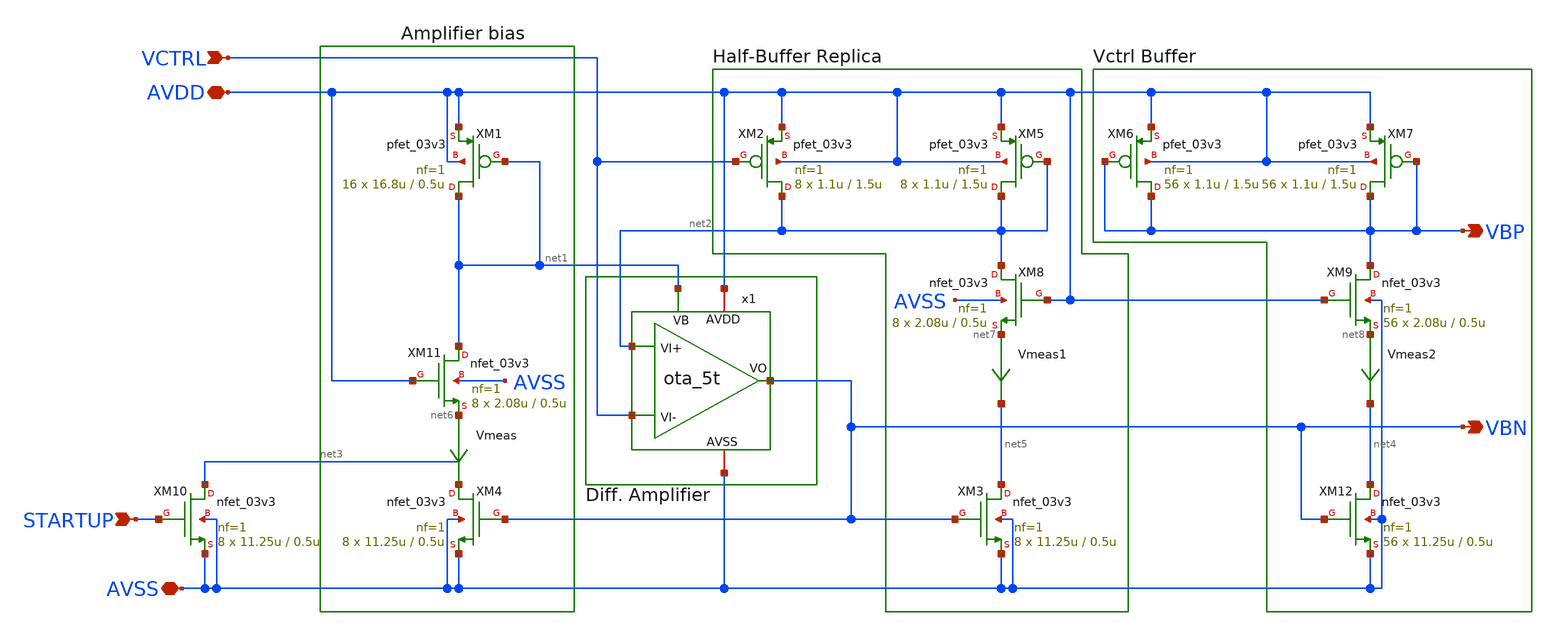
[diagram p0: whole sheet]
** sch_path: designs/libs/core_analog/bias_generator/bias_generator.sch
**.subckt bias_generator VCTRL STARTUP AVDD AVSS VBP VBN
*.ipin VCTRL
*.ipin STARTUP
*.iopin AVDD
*.iopin AVSS
*.opin VBP
*.opin VBN
x1 VBN AVDD net2 VCTRL AVSS net1 ota_5t
Vmeas net6 net3 0
.save i(vmeas)
Vmeas1 net7 net5 0
.save i(vmeas1)
Vmeas2 net8 net4 0
.save i(vmeas2)
XM1 net1 net1 AVDD AVDD pfet_03v3 L=0.5u W=16.8u nf=1 ad='int((nf+1)/2) * W/nf * 0.18u' as='int((nf+2)/2) * W/nf * 0.18u'
+ pd='2*int((nf+1)/2) * (W/nf + 0.18u)' ps='2*int((nf+2)/2) * (W/nf + 0.18u)' nrd='0.18u / W' nrs='0.18u / W'
+ sa=0 sb=0 sd=0 m=16
XM8 net2 AVDD net7 AVSS nfet_03v3 L=0.5u W=2.08u nf=1 ad='int((nf+1)/2) * W/nf * 0.18u' as='int((nf+2)/2) * W/nf * 0.18u'
+ pd='2*int((nf+1)/2) * (W/nf + 0.18u)' ps='2*int((nf+2)/2) * (W/nf + 0.18u)' nrd='0.18u / W' nrs='0.18u / W'
+ sa=0 sb=0 sd=0 m=8
XM9 VBP AVDD net8 AVSS nfet_03v3 L=0.5u W=2.08u nf=1 ad='int((nf+1)/2) * W/nf * 0.18u' as='int((nf+2)/2) * W/nf * 0.18u'
+ pd='2*int((nf+1)/2) * (W/nf + 0.18u)' ps='2*int((nf+2)/2) * (W/nf + 0.18u)' nrd='0.18u / W' nrs='0.18u / W'
+ sa=0 sb=0 sd=0 m=56
XM11 net1 AVDD net6 AVSS nfet_03v3 L=0.5u W=2.08u nf=1 ad='int((nf+1)/2) * W/nf * 0.18u' as='int((nf+2)/2) * W/nf * 0.18u'
+ pd='2*int((nf+1)/2) * (W/nf + 0.18u)' ps='2*int((nf+2)/2) * (W/nf + 0.18u)' nrd='0.18u / W' nrs='0.18u / W'
+ sa=0 sb=0 sd=0 m=8
XM12 net4 VBN AVSS AVSS nfet_03v3 L=0.5u W=11.25u nf=1 ad='int((nf+1)/2) * W/nf * 0.18u' as='int((nf+2)/2) * W/nf * 0.18u'
+ pd='2*int((nf+1)/2) * (W/nf + 0.18u)' ps='2*int((nf+2)/2) * (W/nf + 0.18u)' nrd='0.18u / W' nrs='0.18u / W'
+ sa=0 sb=0 sd=0 m=56
XM3 net5 VBN AVSS AVSS nfet_03v3 L=0.5u W=11.25u nf=1 ad='int((nf+1)/2) * W/nf * 0.18u' as='int((nf+2)/2) * W/nf * 0.18u'
+ pd='2*int((nf+1)/2) * (W/nf + 0.18u)' ps='2*int((nf+2)/2) * (W/nf + 0.18u)' nrd='0.18u / W' nrs='0.18u / W'
+ sa=0 sb=0 sd=0 m=8
XM4 net3 VBN AVSS AVSS nfet_03v3 L=0.5u W=11.25u nf=1 ad='int((nf+1)/2) * W/nf * 0.18u' as='int((nf+2)/2) * W/nf * 0.18u'
+ pd='2*int((nf+1)/2) * (W/nf + 0.18u)' ps='2*int((nf+2)/2) * (W/nf + 0.18u)' nrd='0.18u / W' nrs='0.18u / W'
+ sa=0 sb=0 sd=0 m=8
XM10 net3 STARTUP AVSS AVSS nfet_03v3 L=0.5u W=11.25u nf=1 ad='int((nf+1)/2) * W/nf * 0.18u' as='int((nf+2)/2) * W/nf * 0.18u'
+ pd='2*int((nf+1)/2) * (W/nf + 0.18u)' ps='2*int((nf+2)/2) * (W/nf + 0.18u)' nrd='0.18u / W' nrs='0.18u / W'
+ sa=0 sb=0 sd=0 m=8
XM2 net2 VCTRL AVDD AVDD pfet_03v3 L=1.5u W=1.1u nf=1 ad='int((nf+1)/2) * W/nf * 0.18u' as='int((nf+2)/2) * W/nf * 0.18u'
+ pd='2*int((nf+1)/2) * (W/nf + 0.18u)' ps='2*int((nf+2)/2) * (W/nf + 0.18u)' nrd='0.18u / W' nrs='0.18u / W'
+ sa=0 sb=0 sd=0 m=8
XM5 net2 net2 AVDD AVDD pfet_03v3 L=1.5u W=1.1u nf=1 ad='int((nf+1)/2) * W/nf * 0.18u' as='int((nf+2)/2) * W/nf * 0.18u'
+ pd='2*int((nf+1)/2) * (W/nf + 0.18u)' ps='2*int((nf+2)/2) * (W/nf + 0.18u)' nrd='0.18u / W' nrs='0.18u / W'
+ sa=0 sb=0 sd=0 m=8
XM6 VBP VBP AVDD AVDD pfet_03v3 L=1.5u W=1.1u nf=1 ad='int((nf+1)/2) * W/nf * 0.18u' as='int((nf+2)/2) * W/nf * 0.18u'
+ pd='2*int((nf+1)/2) * (W/nf + 0.18u)' ps='2*int((nf+2)/2) * (W/nf + 0.18u)' nrd='0.18u / W' nrs='0.18u / W'
+ sa=0 sb=0 sd=0 m=56
XM7 VBP VBP AVDD AVDD pfet_03v3 L=1.5u W=1.1u nf=1 ad='int((nf+1)/2) * W/nf * 0.18u' as='int((nf+2)/2) * W/nf * 0.18u'
+ pd='2*int((nf+1)/2) * (W/nf + 0.18u)' ps='2*int((nf+2)/2) * (W/nf + 0.18u)' nrd='0.18u / W' nrs='0.18u / W'
+ sa=0 sb=0 sd=0 m=56
**.ends

* expanding   symbol:  libs/core_analog/ota_5t/ota_5t.sym # of pins=6
** sym_path: designs/libs/core_analog/ota_5t/ota_5t.sym
** sch_path: designs/libs/core_analog/ota_5t/ota_5t.sch
.subckt ota_5t VO AVDD VI+ VI- AVSS VB
*.ipin VI+
*.ipin VI-
*.ipin VB
*.iopin AVDD
*.iopin AVSS
*.opin VO
XM1 VO VI- net2 AVDD pfet_03v3 L=0.5u W=6.55u nf=1 ad='int((nf+1)/2) * W/nf * 0.18u' as='int((nf+2)/2) * W/nf * 0.18u'
+ pd='2*int((nf+1)/2) * (W/nf + 0.18u)' ps='2*int((nf+2)/2) * (W/nf + 0.18u)' nrd='0.18u / W' nrs='0.18u / W'
+ sa=0 sb=0 sd=0 m=8
XM4 VO net1 AVSS AVSS nfet_03v3 L=0.5u W=4.8u nf=1 ad='int((nf+1)/2) * W/nf * 0.18u' as='int((nf+2)/2) * W/nf * 0.18u'
+ pd='2*int((nf+1)/2) * (W/nf + 0.18u)' ps='2*int((nf+2)/2) * (W/nf + 0.18u)' nrd='0.18u / W' nrs='0.18u / W'
+ sa=0 sb=0 sd=0 m=4
XM3 net2 VB net3 AVDD pfet_03v3 L=0.5u W=16.8u nf=1 ad='int((nf+1)/2) * W/nf * 0.18u' as='int((nf+2)/2) * W/nf * 0.18u'
+ pd='2*int((nf+1)/2) * (W/nf + 0.18u)' ps='2*int((nf+2)/2) * (W/nf + 0.18u)' nrd='0.18u / W' nrs='0.18u / W'
+ sa=0 sb=0 sd=0 m=16
XM2 net1 VI+ net2 AVDD pfet_03v3 L=0.5u W=6.55u nf=1 ad='int((nf+1)/2) * W/nf * 0.18u' as='int((nf+2)/2) * W/nf * 0.18u'
+ pd='2*int((nf+1)/2) * (W/nf + 0.18u)' ps='2*int((nf+2)/2) * (W/nf + 0.18u)' nrd='0.18u / W' nrs='0.18u / W'
+ sa=0 sb=0 sd=0 m=8
XM5 net1 net1 AVSS AVSS nfet_03v3 L=0.5u W=4.8u nf=1 ad='int((nf+1)/2) * W/nf * 0.18u' as='int((nf+2)/2) * W/nf * 0.18u'
+ pd='2*int((nf+1)/2) * (W/nf + 0.18u)' ps='2*int((nf+2)/2) * (W/nf + 0.18u)' nrd='0.18u / W' nrs='0.18u / W'
+ sa=0 sb=0 sd=0 m=4
Vmeas AVDD net3 0
.save i(vmeas)
.ends

.end
